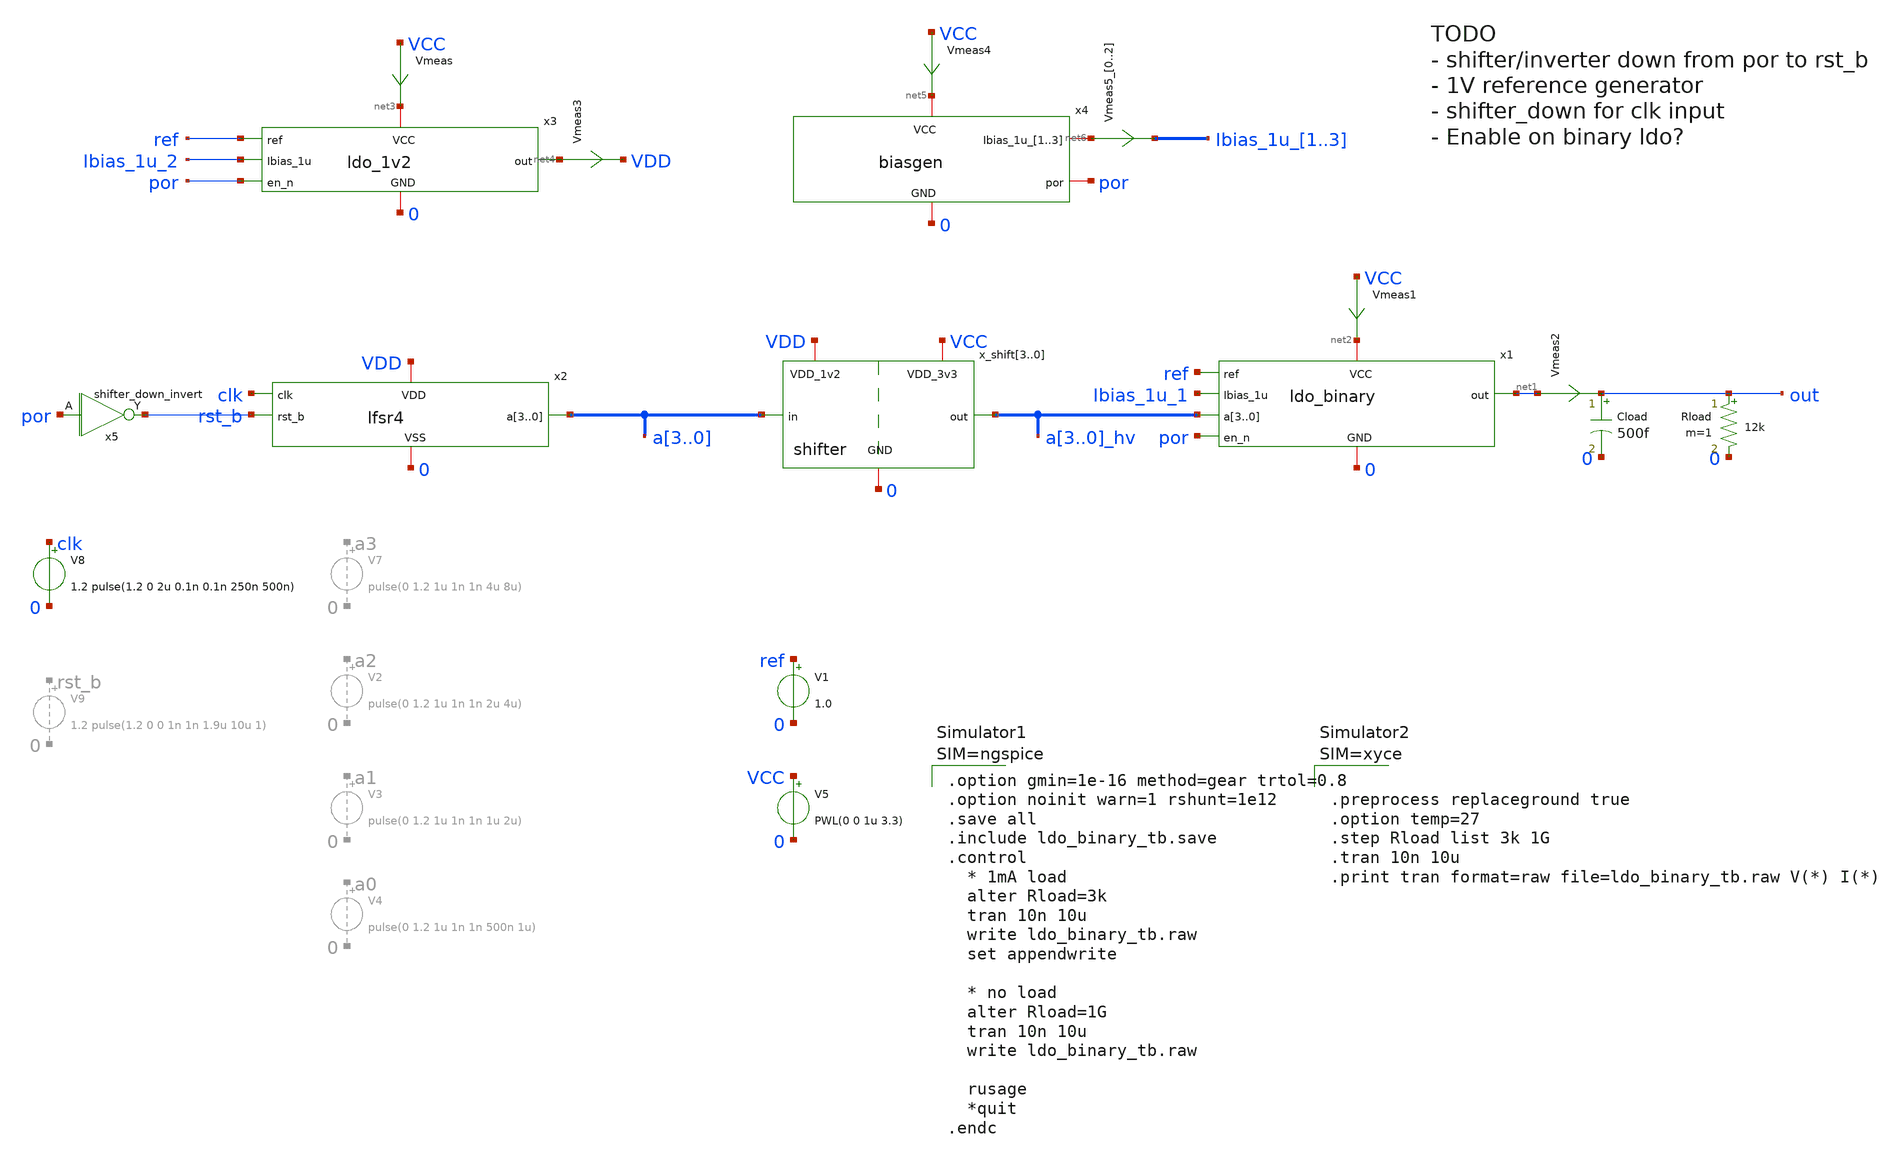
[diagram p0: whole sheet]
** sch_path: FLDO/design_data/xschem/ldo_binary_tb.sch
* IHP-GmbH/IHP-Open-PDK/ihp-sg13g2/libs.tech/xschem/sg13g2_stdcells/sg13g2_buf_4.sch:
* Copyright 2023 IHP PDK Authors
* Licensed under the Apache License, Version 2.0 (the "License");
**.subckt ldo_binary_tb
x_shift3 VCC VDD 0 a3 a3_hv shifter
x_shift2 VCC VDD 0 a2 a2_hv shifter
x_shift1 VCC VDD 0 a1 a1_hv shifter
x_shift0 VCC VDD 0 a0 a0_hv shifter
V5 VCC 0 PWL(0 0 1u 3.3)
Cload out 0 500f m=1
Rload out 0 12k m=1
x1 net2 0 ref Ibias_1u_1 net1 a3_hv a2_hv a1_hv a0_hv por ldo_binary
V1 ref 0 1.0
x2 VDD 0 clk rst_b a3 a2 a1 a0 lfsr4
V8 clk 0 1.2 pulse(1.2 0 2u 0.1n 0.1n 250n 500n)
x3 net3 0 ref Ibias_1u_2 net4 por ldo_1v2
Vmeas VCC net3 0
.save i(vmeas)
Vmeas1 VCC net2 0
.save i(vmeas1)
Vmeas2 net1 out 0
.save i(vmeas2)
Vmeas3 net4 VDD 0
.save i(vmeas3)
x4 net5 0 net6[2] net6[1] net6[0] por biasgen
Vmeas4 VCC net5 0
.save i(vmeas4)
Vmeas5_0 net6[2] Ibias_1u_1 0
Vmeas5_1 net6[1] Ibias_1u_2 0
Vmeas5_2 net6[0] Ibias_1u_3 0
.save i(vmeas5_0)
.save i(vmeas5_1)
.save i(vmeas5_2)
x5 rst_b por VDD 0 shifter_down_invert
**** begin user architecture code









** IHP models
.lib cornerMOSlv.lib mos_tt
.lib cornerMOShv.lib mos_tt
.lib cornerHBT.lib hbt_typ
.lib cornerRES.lib res_typ
.lib cornerCAP.lib cap_typ

.include sg13g2_stdcell.spice






.option gmin=1e-16 method=gear trtol=0.8
.option noinit warn=1 rshunt=1e12
.save all
.include ldo_binary_tb.save
.control
  * 1mA load
  alter Rload=3k
  tran 10n 10u
  write ldo_binary_tb.raw
  set appendwrite

  * no load
  alter Rload=1G
  tran 10n 10u
  write ldo_binary_tb.raw

  rusage
  *quit
.endc



**** end user architecture code
**.ends

* expanding   symbol:  shifter.sym # of pins=5
** sym_path: FLDO/design_data/xschem/shifter.sym
** sch_path: FLDO/design_data/xschem/shifter.sch
.subckt shifter VDD_3v3 VDD_1v2 GND in out
*.iopin VDD_3v3
*.iopin VDD_1v2
*.iopin GND
*.ipin in
*.opin out
XM1 lvlsh in_b GND GND sg13_hv_nmos w=2u l=0.45u ng=1 m=1 mm_ok=1
XM2 lvlsh_b in GND GND sg13_hv_nmos w=2u l=0.45u ng=1 m=1 mm_ok=1
XM3 lvlsh lvlsh_b VDD_3v3 VDD_3v3 sg13_hv_pmos w=0.3u l=0.45u ng=1 m=1 mm_ok=1
XM4 lvlsh_b lvlsh VDD_3v3 VDD_3v3 sg13_hv_pmos w=0.3u l=0.45u ng=1 m=1 mm_ok=1
XM5 in_b in GND GND sg13_lv_nmos w=0.74u l=0.13u ng=1 m=1 mm_ok=1
XM6 in_b in VDD_1v2 VDD_1v2 sg13_lv_pmos w=1.12u l=0.13u ng=1 m=1 mm_ok=1
XM7 out lvlsh_b GND GND sg13_hv_nmos w=2u l=0.45u ng=1 m=1 mm_ok=1
XM8 out lvlsh_b VDD_3v3 VDD_3v3 sg13_hv_pmos w=2u l=0.4u ng=1 m=2 mm_ok=1
.ends


* expanding   symbol:  ldo_binary.sym # of pins=7
** sym_path: FLDO/design_data/xschem/ldo_binary.sym
** sch_path: FLDO/design_data/xschem/ldo_binary.sch
.subckt ldo_binary VCC GND ref Ibias_1u out a3 a2 a1 a0 en_n
*.iopin VCC
*.iopin GND
*.ipin ref
*.ipin Ibias_1u
*.opin out
*.ipin a3,a2,a1,a0
*.ipin en_n
XR4 net1 out GND rhigh w=0.5e-6 l=12e-6 m=1 b=0
XM1 net1 a0 out VCC sg13_hv_pmos w=2u l=0.4u ng=1 m=1 mm_ok=1
XM2 net2 a1 net1 VCC sg13_hv_pmos w=2u l=0.4u ng=1 m=1 mm_ok=1
XM3 net3 a2 net2 VCC sg13_hv_pmos w=2u l=0.4u ng=1 m=1 mm_ok=1
XM4 out vg net4 net4 sg13_hv_pmos w=100u l=0.4u ng=10 m=1 mm_ok=1
Vmeas VCC net4 0
.save i(vmeas)
XC1 out vg cap_cmim w=10.0e-6 l=10.0e-6 m=1
XM11 net5 a3 net3 VCC sg13_hv_pmos w=2u l=0.4u ng=1 m=1 mm_ok=1
XM15 vg en VCC VCC sg13_hv_pmos w=0.3u l=0.4u ng=1 m=1 mm_ok=1
x1 VCC GND Ibias_1u fb ref vg ldo_ota
XM5 Ibias_1u en_n GND GND sg13_hv_nmos w=0.3u l=0.45u ng=1 m=1 mm_ok=1
XM6 en en_n GND GND sg13_hv_nmos w=0.3u l=0.45u ng=1 m=1 mm_ok=1
XM7 en en_n VCC VCC sg13_hv_pmos w=0.3u l=0.4u ng=1 m=1 mm_ok=1
XRdummy GND GND gnd rhigh w=0.5e-6 l=12e-6 m=5 b=0
XR2 net2 net1 GND rhigh w=0.5e-6 l=2*12e-6 m=1 b=0
XR6 net3 net2 GND rhigh w=0.5e-6 l=4*12e-6 m=1 b=0
XR5 net5 net3 GND rhigh w=0.5e-6 l=8*12e-6 m=1 b=0
XR3 fb net5 GND rhigh w=0.5e-6 l=6*12e-6 m=1 b=0
XR1 GND fb GND rhigh w=0.5e-6 l=10*12e-6 m=1 b=0
.ends


* expanding   symbol:  lfsr4.sym # of pins=5
** sym_path: FLDO/design_data/xschem/lfsr4.sym
** sch_path: FLDO/design_data/xschem/lfsr4.sch
.subckt lfsr4 VDD VSS clk rst_b a3 a2 a1 a0
*.iopin VDD
*.ipin clk
*.iopin VSS
*.ipin rst_b
*.opin a3,a2,a1,a0
x1 d2 a3 a0 VDD VSS sg13g2_xnor2_1
x2 a3 net2 net1 a0 rst_b VDD VSS sg13g2_dfrbp_1
x3 a2 net3 net1 d2 rst_b VDD VSS sg13g2_dfrbp_1
x4 a1 net4 net1 a2 rst_b VDD VSS sg13g2_dfrbp_1
x5 a0 net5 net1 a1 rst_b VDD VSS sg13g2_dfrbp_1
x6 net1 clk VDD VSS sg13g2_buf_4
x7[0] VDD VSS sg13g2_decap_8
x7[1] VDD VSS sg13g2_decap_8
x7[2] VDD VSS sg13g2_decap_8
x7[3] VDD VSS sg13g2_decap_8
.ends


* expanding   symbol:  ldo_1v2.sym # of pins=6
** sym_path: FLDO/design_data/xschem/ldo_1v2.sym
** sch_path: FLDO/design_data/xschem/ldo_1v2.sch
.subckt ldo_1v2 VCC GND ref Ibias_1u out en_n
*.iopin VCC
*.iopin GND
*.ipin ref
*.ipin Ibias_1u
*.opin out
*.ipin en_n
XM4 out vg net1 net1 sg13_hv_pmos w=50u l=0.4u ng=10 m=1 mm_ok=1
Vmeas VCC net1 0
.save i(vmeas)
XC1 out vg cap_cmim w=10.0e-6 l=10.0e-6 m=1
XM2 Ibias_1u en_n GND GND sg13_hv_nmos w=0.3u l=0.45u ng=1 m=1 mm_ok=1
XM3 vg en VCC VCC sg13_hv_pmos w=0.3u l=0.4u ng=1 m=1 mm_ok=1
XM1 en en_n GND GND sg13_hv_nmos w=0.3u l=0.45u ng=1 m=1 mm_ok=1
XM11 en en_n VCC VCC sg13_hv_pmos w=0.3u l=0.4u ng=1 m=1 mm_ok=1
XRdummy GND GND gnd rhigh w=0.5e-6 l=4e-6 m=2 b=0 mm_ok=1
x1 VCC GND Ibias_1u fb ref vg ldo_ota
XR2 fb out gnd rhigh w=0.5e-6 l=4*4e-6 m=1 b=0
XR1 GND fb gnd rhigh w=0.5e-6 l=20*4e-6 m=1 b=0
.ends


* expanding   symbol:  biasgen.sym # of pins=4
** sym_path: FLDO/design_data/xschem/biasgen.sym
** sch_path: FLDO/design_data/xschem/biasgen.sch
.subckt biasgen VCC GND Ibias_1u_1 Ibias_1u_2 Ibias_1u_3 por
*.iopin VCC
*.iopin GND
*.iopin Ibias_1u_1,Ibias_1u_2,Ibias_1u_3
*.opin por
XM1 vp vn net1 GND sg13_hv_nmos w=2u l=2u ng=1 m=3 mm_ok=1
XM2 vn vn GND GND sg13_hv_nmos w=2u l=2u ng=1 m=1 mm_ok=1
XM3 vn vp VCC VCC sg13_hv_pmos w=0.5u l=2u ng=1 m=2 mm_ok=1
XM4 vp vp VCC VCC sg13_hv_pmos w=0.5u l=2u ng=1 m=2 mm_ok=1
XMout0 Ibias_1u_0 vp VCC VCC sg13_hv_pmos w=0.5u l=2u ng=1 m=1 mm_ok=1
XMout1 Ibias_1u_1 vp VCC VCC sg13_hv_pmos w=0.5u l=2u ng=1 m=1 mm_ok=1
XMout2 Ibias_1u_2 vp VCC VCC sg13_hv_pmos w=0.5u l=2u ng=1 m=1 mm_ok=1
XMout3 Ibias_1u_3 vp VCC VCC sg13_hv_pmos w=0.5u l=2u ng=1 m=1 mm_ok=1
XC1 Ibias_1u_0 GND cap_cmim w=7.0e-6 l=7.0e-6 m=1
XM7 por Ibias_1u_0 VCC VCC sg13_hv_pmos w=0.3u l=0.4u ng=1 m=1 mm_ok=1
XM8 por Ibias_1u_0 GND GND sg13_hv_nmos w=0.3u l=0.45u ng=1 m=1 mm_ok=1
XR1 net1 GND GND rppd w=0.5e-6 l=80e-6 m=1 b=0 mm_ok=1
XM5 vp vstart GND GND sg13_hv_nmos w=0.3u l=0.45u ng=1 m=1 mm_ok=1
XM6 vstart vn GND GND sg13_hv_nmos w=0.3u l=0.45u ng=1 m=1 mm_ok=1
XM9 vstart vn net2 VCC sg13_hv_pmos w=0.3u l=2u ng=1 m=1 mm_ok=1
XM10 net2 net2 net3 VCC sg13_hv_pmos w=0.3u l=2u ng=1 m=1 mm_ok=1
XM11 net3 net3 VCC VCC sg13_hv_pmos w=0.3u l=2u ng=1 m=1 mm_ok=1
.ends


* expanding   symbol:  shifter_down_invert.sym # of pins=2
** sym_path: FLDO/design_data/xschem/shifter_down_invert.sym
** sch_path: FLDO/design_data/xschem/shifter_down_invert.sch
.subckt shifter_down_invert Y A VDD VSS
*.opin Y
*.ipin A
XM1 Y A VSS VSS sg13_hv_nmos w=0.3u l=0.45u ng=1 m=1 mm_ok=1
XM2 Y A VDD VDD sg13_hv_pmos w=0.3u l=0.4u ng=1 m=1 mm_ok=1
.ends


* expanding   symbol:  ldo_ota.sym # of pins=6
** sym_path: FLDO/design_data/xschem/ldo_ota.sym
** sch_path: FLDO/design_data/xschem/ldo_ota.sch
.subckt ldo_ota VCC GND Ibias_1u plus min out
*.iopin VCC
*.iopin GND
*.ipin plus
*.ipin min
*.opin out
*.ipin Ibias_1u
XM5 vbp plus tail GND sg13_hv_nmos w=3u l=2u ng=3 m=1 mm_ok=1
XM6 out min tail GND sg13_hv_nmos w=3u l=2u ng=3 m=1 mm_ok=1
XM7 tail Ibias_1u GND GND sg13_hv_nmos w=1u l=2u ng=1 m=2 mm_ok=1
XM8 Ibias_1u Ibias_1u GND GND sg13_hv_nmos w=1u l=2u ng=1 m=1 mm_ok=1
XM9 out vbp VCC VCC sg13_hv_pmos w=2u l=2u ng=2 m=1 mm_ok=1
XM10 vbp vbp VCC VCC sg13_hv_pmos w=2u l=2u ng=2 m=1 mm_ok=1
XMdummy0 GND Ibias_1u GND GND sg13_hv_nmos w=1u l=2u ng=1 m=2 mm_ok=1
XMdummy1 tail tail tail GND sg13_hv_nmos w=1u l=2u ng=1 m=4 mm_ok=1
XMdummyP VCC vbp VCC VCC sg13_hv_pmos w=1u l=2u ng=1 m=2 mm_ok=1
.ends


* expanding   symbol:  sg13g2_stdcells/sg13g2_xnor2_1.sym # of pins=3
** sym_path: sg13g2_stdcells/sg13g2_xnor2_1.sym
** sch_path: sg13g2_stdcells/sg13g2_xnor2_1.sch
.subckt sg13g2_xnor2_1 Y A B VDD VSS
*.ipin A
*.opin Y
*.ipin B
*.iopin VDD
*.iopin VSS
XM1 net1 B net4 VSS sg13_lv_nmos w=640.00n l=130.00n ng=1 m=1 mm_ok=1
XM2 net4 A VSS VSS sg13_lv_nmos w=640.00n l=130.00n ng=1 m=1 mm_ok=1
XM3 net2 A VSS VSS sg13_lv_nmos w=740.00n l=130.00n ng=1 m=1 mm_ok=1
XM4 Y net1 net2 VSS sg13_lv_nmos w=740.00n l=130.00n ng=1 m=1 mm_ok=1
XM5 net2 B VSS VSS sg13_lv_nmos w=740.00n l=130.00n ng=1 m=1 mm_ok=1
XM6 net1 A VDD VDD sg13_lv_pmos w=840.00n l=130.00n ng=1 m=1 mm_ok=1
XM7 net1 B VDD VDD sg13_lv_pmos w=840.00n l=130.00n ng=1 m=1 mm_ok=1
XM8 net3 A VDD VDD sg13_lv_pmos w=1.12u l=130.00n ng=1 m=1 mm_ok=1
XM9 Y B net3 VDD sg13_lv_pmos w=1.12u l=130.00n ng=1 m=1 mm_ok=1
XM10 Y net1 VDD VDD sg13_lv_pmos w=1.12u l=130.00n ng=1 m=1 mm_ok=1
.ends


* expanding   symbol:  sg13g2_stdcells/sg13g2_dfrbp_1.sym # of pins=5
** sym_path: sg13g2_stdcells/sg13g2_dfrbp_1.sym
** sch_path: sg13g2_stdcells/sg13g2_dfrbp_1.sch
.subckt sg13g2_dfrbp_1 Q Q_N CLK D RESET_B VDD VSS
*.ipin D
*.ipin RESET_B
*.ipin CLK
*.opin Q
*.opin Q_N
*.iopin VDD
*.iopin VSS
XM1 Db D net10 VSS sg13_lv_nmos w=420.00n l=130.00n ng=1 m=1 mm_ok=1
XM2 net10 RESET_B VSS VSS sg13_lv_nmos w=420.00n l=130.00n ng=1 m=1 mm_ok=1
XM3 net1 clkneg net9 VSS sg13_lv_nmos w=420.00n l=130.00n ng=1 m=1 mm_ok=1
XM4 net9 net1 VSS VSS sg13_lv_nmos w=420.00n l=130.00n ng=1 m=1 mm_ok=1
XM5 net1 net1 net5 VSS sg13_lv_nmos w=420.00n l=130.00n ng=1 m=1 mm_ok=1
XM6 net5 RESET_B VSS VSS sg13_lv_nmos w=420.00n l=130.00n ng=1 m=1 mm_ok=1
XM7 Q_N net1 VSS VSS sg13_lv_nmos w=740.00n l=130.00n ng=1 m=1 mm_ok=1
XM8 net2 net1 VSS VSS sg13_lv_nmos w=740.00n l=130.00n ng=1 m=1 mm_ok=1
XM9 Q net2 VSS VSS sg13_lv_nmos w=740.00n l=130.00n ng=1 m=1 mm_ok=1
XM10 clkneg CLK VSS VSS sg13_lv_nmos w=740.00n l=130.00n ng=1 m=1 mm_ok=1
XM11 clkpos clkneg VSS VSS sg13_lv_nmos w=740.00n l=130.00n ng=1 m=1 mm_ok=1
XM12 Db clkneg net3 VSS sg13_lv_nmos w=420.00n l=130.00n ng=1 m=1 mm_ok=1
XM13 net3 clkpos net8 VSS sg13_lv_nmos w=420.00n l=130.00n ng=1 m=1 mm_ok=1
XM14 net8 net3 net4 VSS sg13_lv_nmos w=420.00n l=130.00n ng=1 m=1 mm_ok=1
XM15 net4 RESET_B VSS VSS sg13_lv_nmos w=420.00n l=130.00n ng=1 m=1 mm_ok=1
XM16 net3 net3 VSS VSS sg13_lv_nmos w=740.00n l=130.00n ng=1 m=1 mm_ok=1
XM17 net3 clkpos net1 VSS sg13_lv_nmos w=740.00n l=130.00n ng=1 m=1 mm_ok=1
XM18 Db RESET_B VDD VDD sg13_lv_pmos w=420.00n l=130.00n ng=1 m=1 mm_ok=1
XM19 Db D VDD VDD sg13_lv_pmos w=420.00n l=130.00n ng=1 m=1 mm_ok=1
XM20 net7 net1 VDD VDD sg13_lv_pmos w=420.00n l=130.00n ng=1 m=1 mm_ok=1
XM21 net1 clkpos net7 VDD sg13_lv_pmos w=420.00n l=130.00n ng=1 m=1 mm_ok=1
XM22 net1 net1 VDD VDD sg13_lv_pmos w=420.00n l=130.00n ng=1 m=1 mm_ok=1
XM23 net1 RESET_B VDD VDD sg13_lv_pmos w=420.00n l=130.00n ng=1 m=1 mm_ok=1
XM24 Q_N net1 VDD VDD sg13_lv_pmos w=1.12u l=130.00n ng=1 m=1 mm_ok=1
XM25 net2 net1 VDD VDD sg13_lv_pmos w=1.12u l=130.00n ng=1 m=1 mm_ok=1
XM26 Q net2 VDD VDD sg13_lv_pmos w=1.12u l=130.00n ng=1 m=1 mm_ok=1
XM27 clkneg CLK VDD VDD sg13_lv_pmos w=1.12u l=130.00n ng=1 m=1 mm_ok=1
XM28 clkpos clkneg VDD VDD sg13_lv_pmos w=1.12u l=130.00n ng=1 m=1 mm_ok=1
XM29 Db clkpos net3 VDD sg13_lv_pmos w=420.00n l=130.00n ng=1 m=1 mm_ok=1
XM30 net6 net3 VDD VDD sg13_lv_pmos w=420.00n l=130.00n ng=1 m=1 mm_ok=1
XM31 net3 clkneg net6 VDD sg13_lv_pmos w=420.00n l=130.00n ng=1 m=1 mm_ok=1
XM32 net3 RESET_B VDD VDD sg13_lv_pmos w=420.00n l=130.00n ng=1 m=1 mm_ok=1
XM33 net3 net3 VDD VDD sg13_lv_pmos w=1.000u l=130.00n ng=1 m=1 mm_ok=1
XM34 net3 clkneg net1 VDD sg13_lv_pmos w=1.000u l=130.00n ng=1 m=1 mm_ok=1
.ends


* expanding   symbol:  sg13g2_stdcells/sg13g2_buf_4.sym # of pins=2
** sym_path: sg13g2_stdcells/sg13g2_buf_4.sym
** sch_path: sg13g2_stdcells/sg13g2_buf_4.sch
.subckt sg13g2_buf_4 X A VDD VSS
*.ipin A
*.opin X
*.iopin VDD
*.iopin VSS
XM1 net1 A VSS VSS sg13_lv_nmos w=740.00n l=130.00n ng=1 m=1 mm_ok=1
XM2 X net1 VSS VSS sg13_lv_nmos w=2.96u l=130.00n ng=4 m=1 mm_ok=1
XM3 net1 A VDD VDD sg13_lv_pmos w=1.68u l=130.00n ng=2 m=1 mm_ok=1
XM4 X net1 VDD VDD sg13_lv_pmos w=4.48u l=130.00n ng=4 m=1 mm_ok=1
.ends


* expanding   symbol:  sg13g2_stdcells/sg13g2_decap_8.sym # of pins=0
** sym_path: sg13g2_stdcells/sg13g2_decap_8.sym
** sch_path: sg13g2_stdcells/sg13g2_decap_8.sch
.subckt sg13g2_decap_8 VDD VSS
*.iopin VDD
*.iopin VSS
XM1 VSS VDD VSS VSS sg13_lv_nmos w=840.00n l=1.000u ng=2 m=1 mm_ok=1
XM2 VDD VSS VDD VDD sg13_lv_pmos w=2.000u l=1.000u ng=2 m=1 mm_ok=1
.ends

.end
